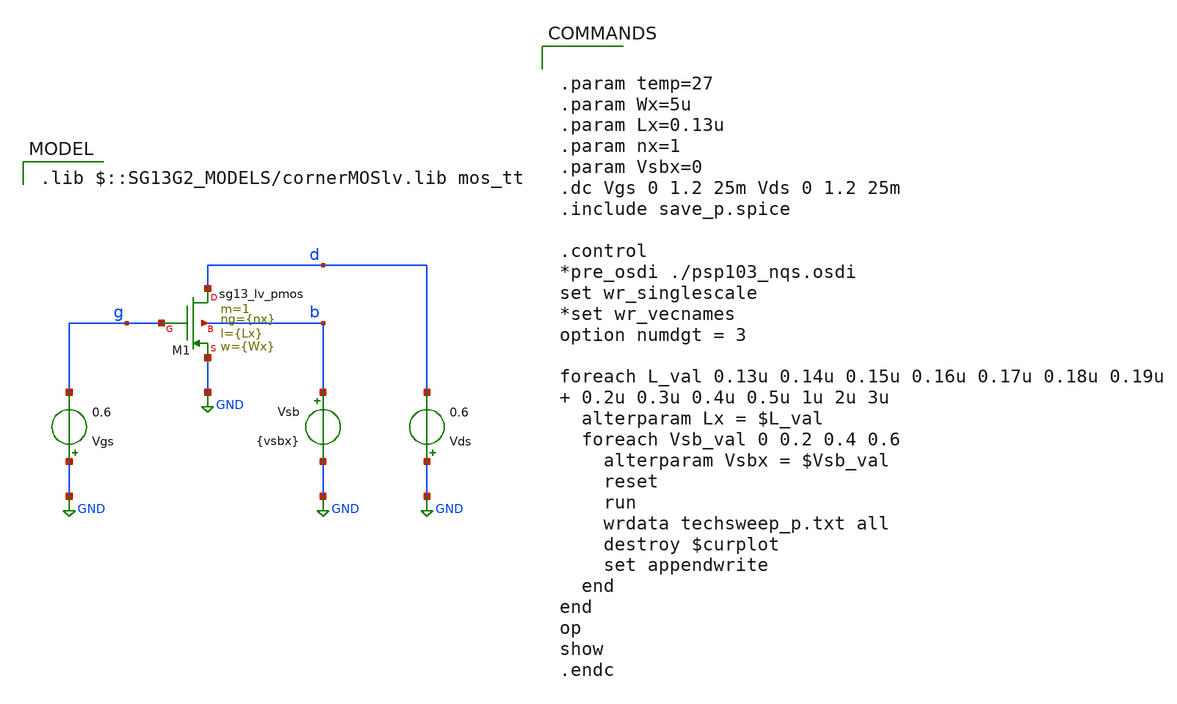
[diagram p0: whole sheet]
** sch_path: 02_gm_id/src/techsweep_p.sch
**.subckt techsweep_p
Vgs GND g 0.6
Vds GND d 0.6
Vsb b GND {vsbx}
XM1 d g GND b sg13_lv_pmos w={Wx} l={Lx} ng={nx} m=1 mm_ok=1
**** begin user architecture code
 .lib $::SG13G2_MODELS/cornerMOSlv.lib mos_tt



.param temp=27
.param Wx=5u
.param Lx=0.13u
.param nx=1
.param Vsbx=0
.dc Vgs 0 1.2 25m Vds 0 1.2 25m
.include save_p.spice

.control
*pre_osdi ./psp103_nqs.osdi
set wr_singlescale
*set wr_vecnames
option numdgt = 3

foreach L_val 0.13u 0.14u 0.15u 0.16u 0.17u 0.18u 0.19u  0.2u 0.3u 0.4u 0.5u 1u 2u 3u
  alterparam Lx = $L_val
  foreach Vsb_val 0 0.2 0.4 0.6
    alterparam Vsbx = $Vsb_val
    reset
    run
    wrdata techsweep_p.txt all
    destroy $curplot
    set appendwrite
  end
end
op
show
.endc


**** end user architecture code
**.ends
.GLOBAL GND
.end
